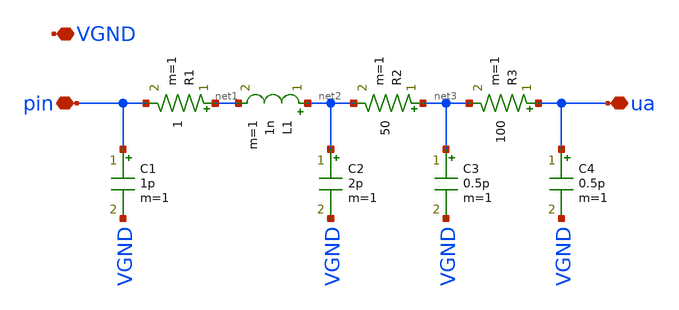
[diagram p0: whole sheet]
** sch_path: xschem/ttgf_analog_pin.sch
**.subckt ttgf_analog_pin ua pin VGND
*.iopin ua
*.iopin pin
*.iopin VGND
R1 net1 pin 1 m=1
C1 pin VGND 1p m=1
L1 net2 net1 1n m=1
R2 net3 net2 50 m=1
R3 ua net3 100 m=1
C2 net2 VGND 2p m=1
C3 net3 VGND 0.5p m=1
C4 ua VGND 0.5p m=1
**.ends
.end
